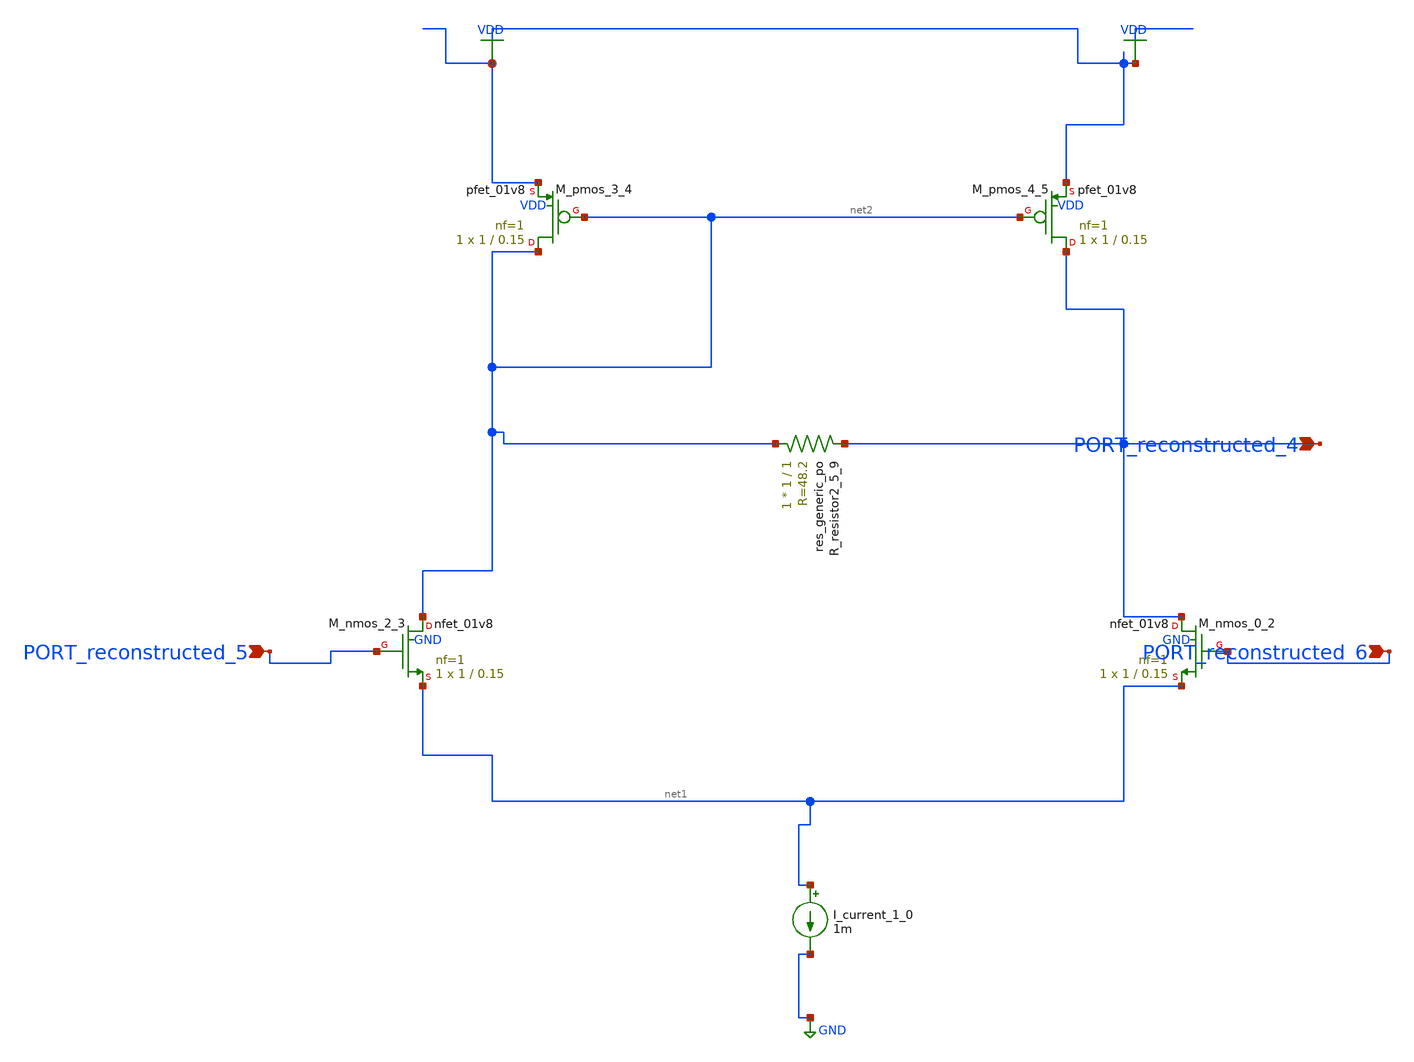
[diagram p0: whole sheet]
** sch_path: schematics/AMSNet/349.sch
**.subckt 349 PORT_reconstructed_5 PORT_reconstructed_6 PORT_reconstructed_4
*.ipin PORT_reconstructed_5
*.ipin PORT_reconstructed_6
*.ipin PORT_reconstructed_4
I_current_1_0 net1 GND 1m
XM_nmos_0_2 PORT_reconstructed_4 PORT_reconstructed_6 net1 GND sky130_fd_pr__nfet_01v8 L=0.15 W=1 nf=1
+ ad='int((1 + 1)/2) * 1 / 1 * 0.29' as='int((1 + 2)/2) * 1 / 1 * 0.29' pd='2*int((1 + 1)/2) * (1 / 1 + 0.29)'
+ ps='2*int((1 + 2)/2) * (1 / 1 + 0.29)' nrd='0.29 / 1 ' nrs='0.29 / 1 ' sa=0 sb=0 sd=0 mult=1 m=1
XM_nmos_2_3 net2 PORT_reconstructed_5 net1 GND sky130_fd_pr__nfet_01v8 L=0.15 W=1 nf=1 ad='int((1 + 1)/2) * 1 / 1 * 0.29'
+ as='int((1 + 2)/2) * 1 / 1 * 0.29' pd='2*int((1 + 1)/2) * (1 / 1 + 0.29)' ps='2*int((1 + 2)/2) * (1 / 1 + 0.29)'
+ nrd='0.29 / 1 ' nrs='0.29 / 1 ' sa=0 sb=0 sd=0 mult=1 m=1
XM_pmos_3_4 net2 net2 VDD VDD sky130_fd_pr__pfet_01v8 L=0.15 W=1 nf=1 ad='int((1 + 1)/2) * 1 / 1 * 0.29'
+ as='int((1 + 2)/2) * 1 / 1 * 0.29' pd='2*int((1 + 1)/2) * (1 / 1 + 0.29)' ps='2*int((1 + 2)/2) * (1 / 1 + 0.29)'
+ nrd='0.29 / 1 ' nrs='0.29 / 1 ' sa=0 sb=0 sd=0 mult=1 m=1
XM_pmos_4_5 PORT_reconstructed_4 net2 VDD VDD sky130_fd_pr__pfet_01v8 L=0.15 W=1 nf=1 ad='int((1 + 1)/2) * 1 / 1 * 0.29'
+ as='int((1 + 2)/2) * 1 / 1 * 0.29' pd='2*int((1 + 1)/2) * (1 / 1 + 0.29)' ps='2*int((1 + 2)/2) * (1 / 1 + 0.29)'
+ nrd='0.29 / 1 ' nrs='0.29 / 1 ' sa=0 sb=0 sd=0 mult=1 m=1
XR_resistor2_5_9 net2 PORT_reconstructed_4 sky130_fd_pr__res_generic_po W=1 L=1 m=1
**.ends
.GLOBAL GND
.GLOBAL VDD
.end
